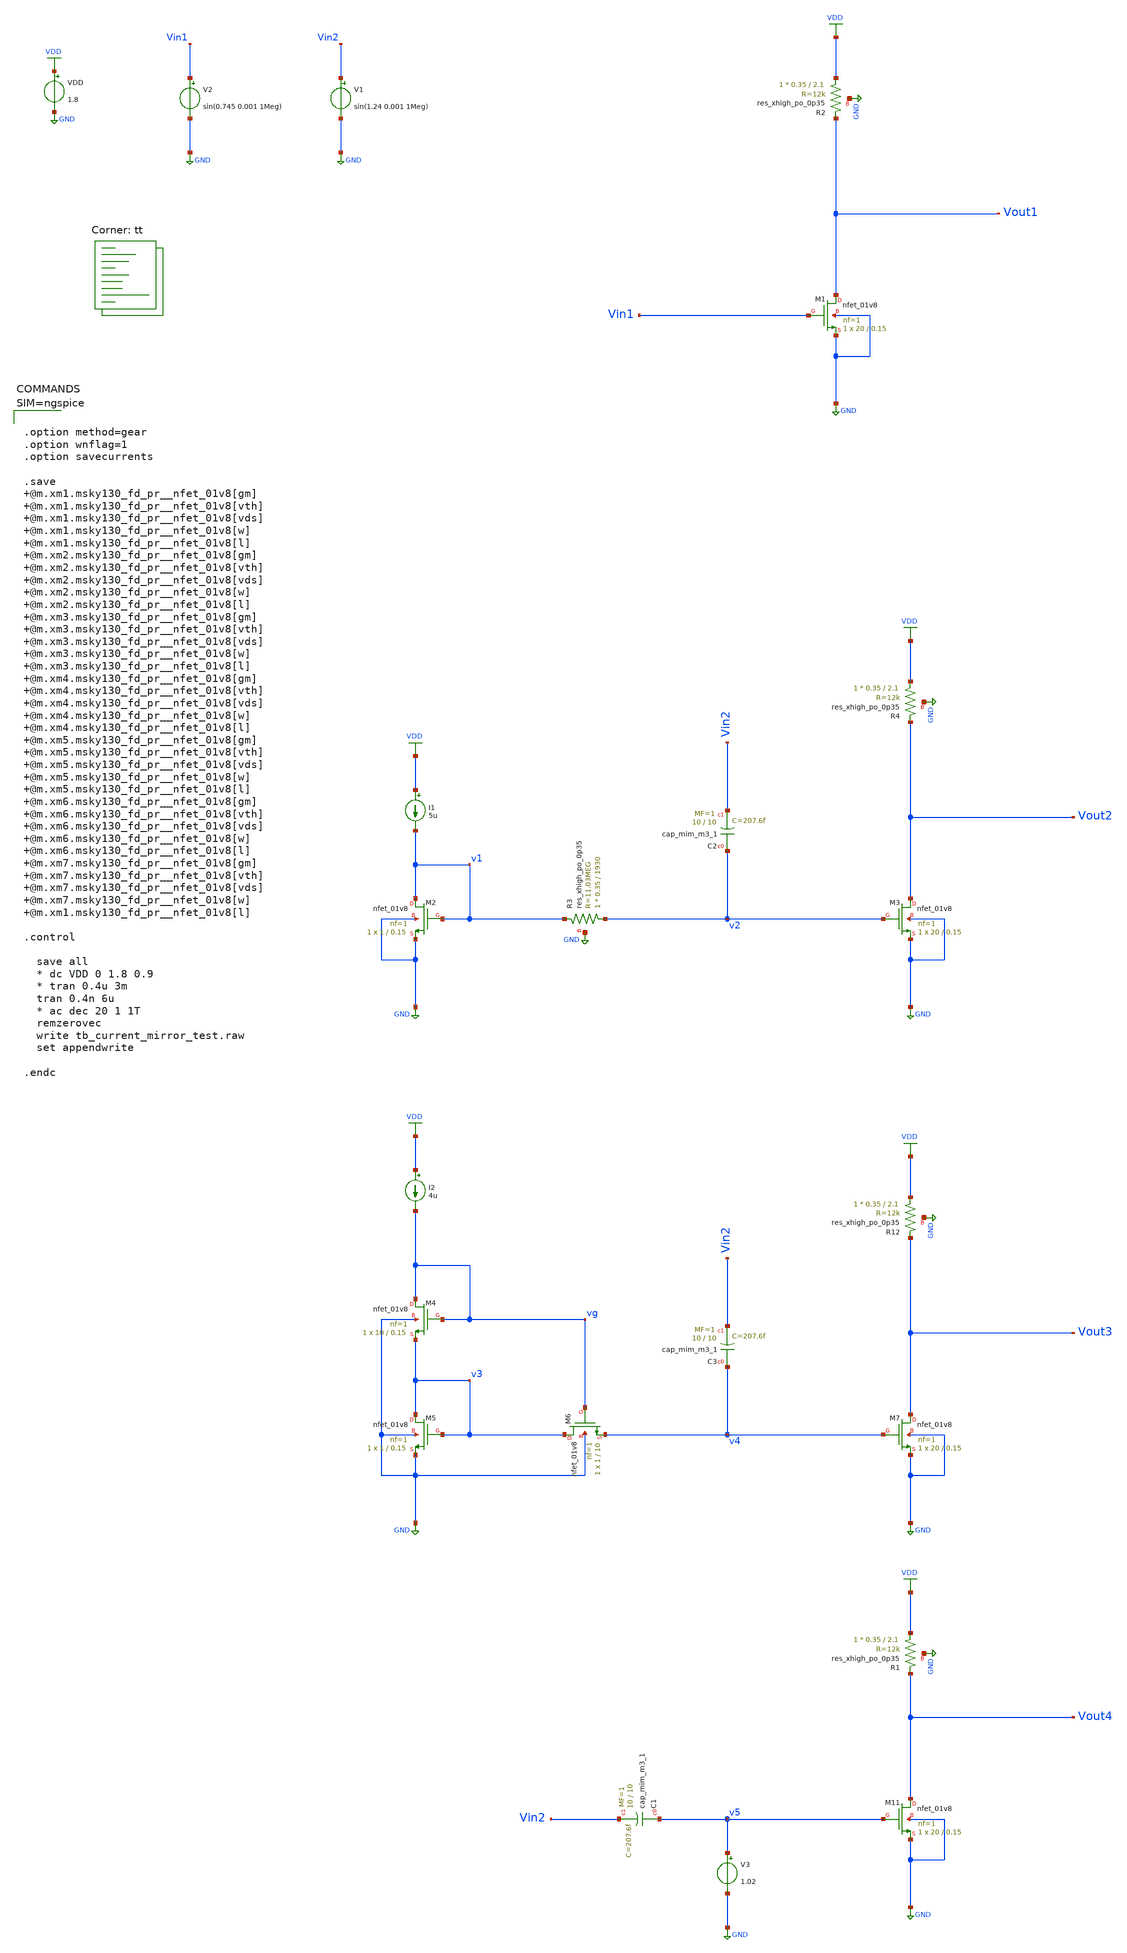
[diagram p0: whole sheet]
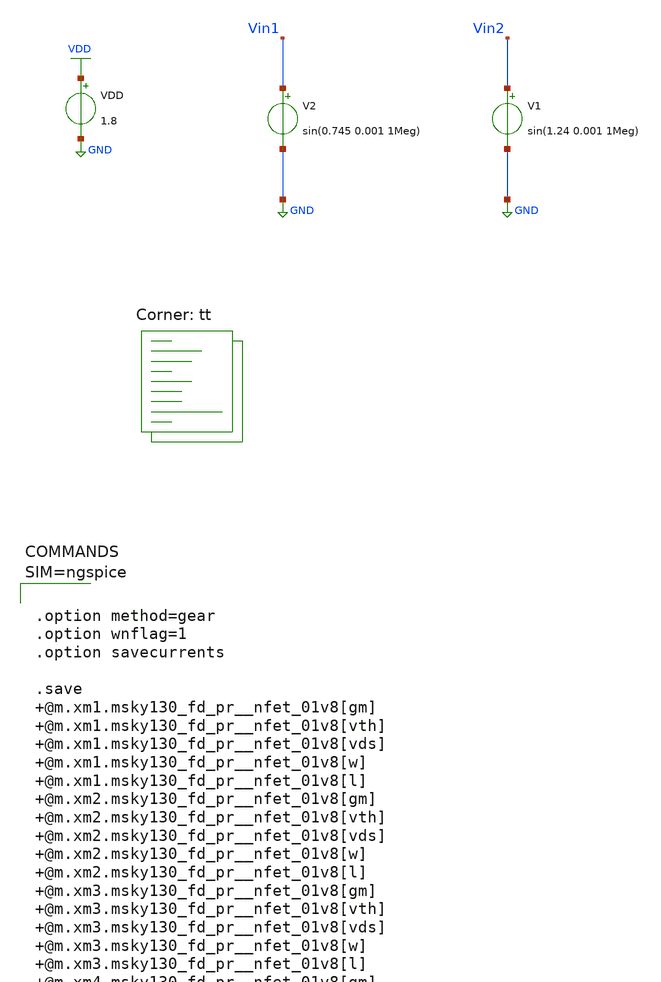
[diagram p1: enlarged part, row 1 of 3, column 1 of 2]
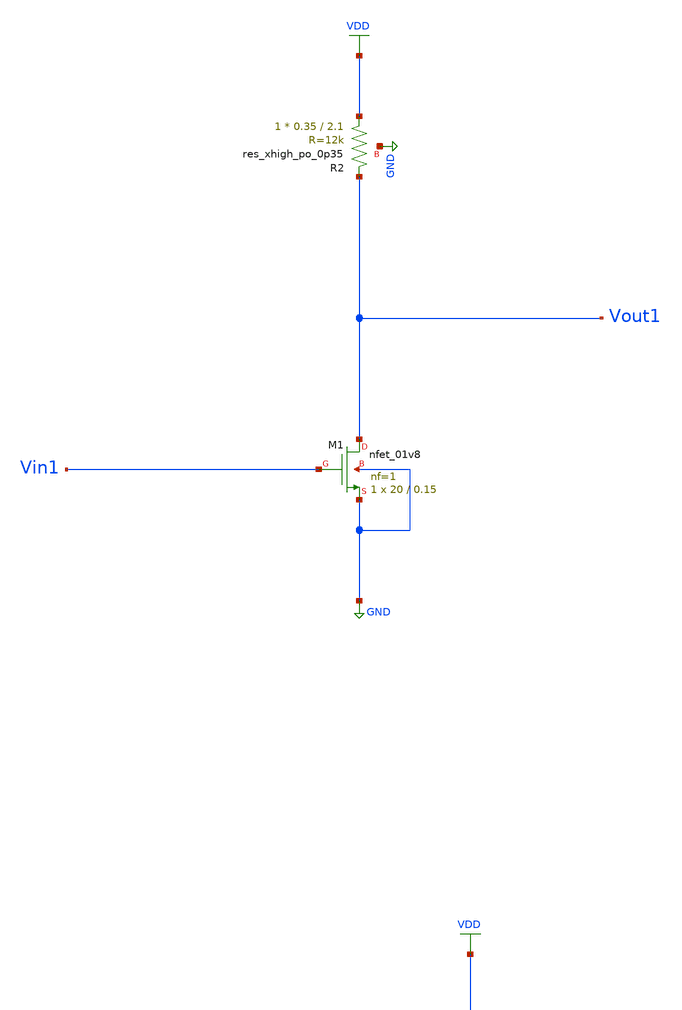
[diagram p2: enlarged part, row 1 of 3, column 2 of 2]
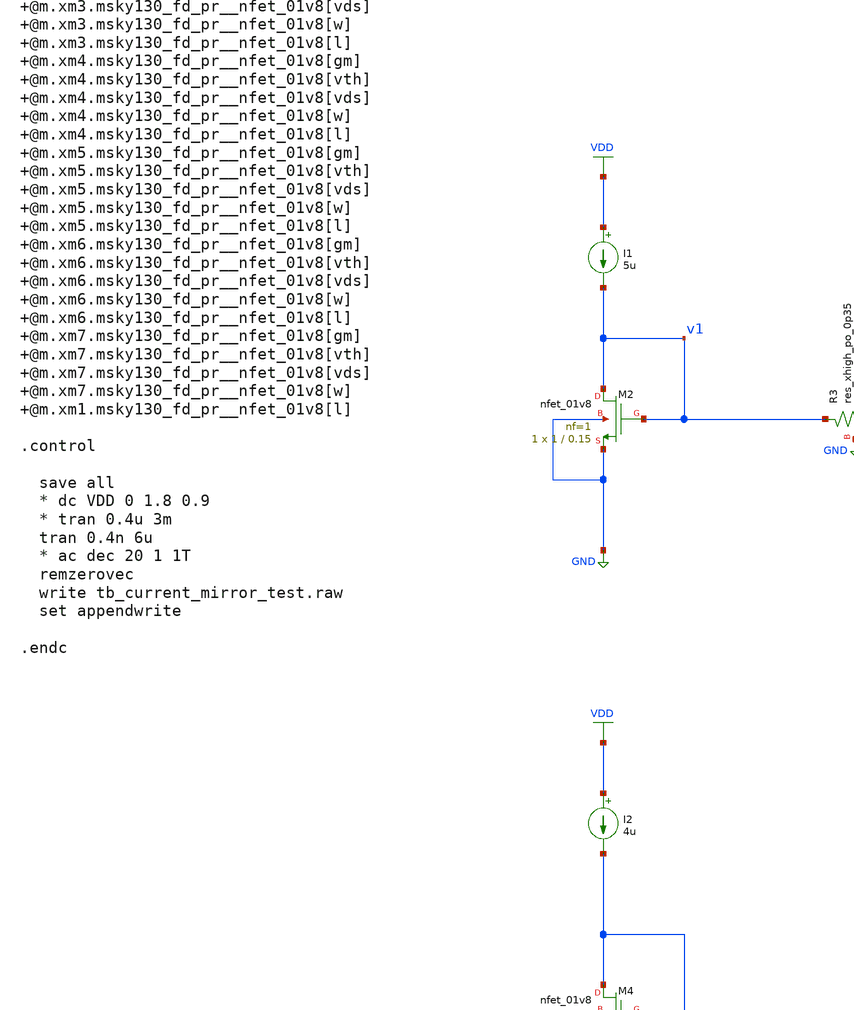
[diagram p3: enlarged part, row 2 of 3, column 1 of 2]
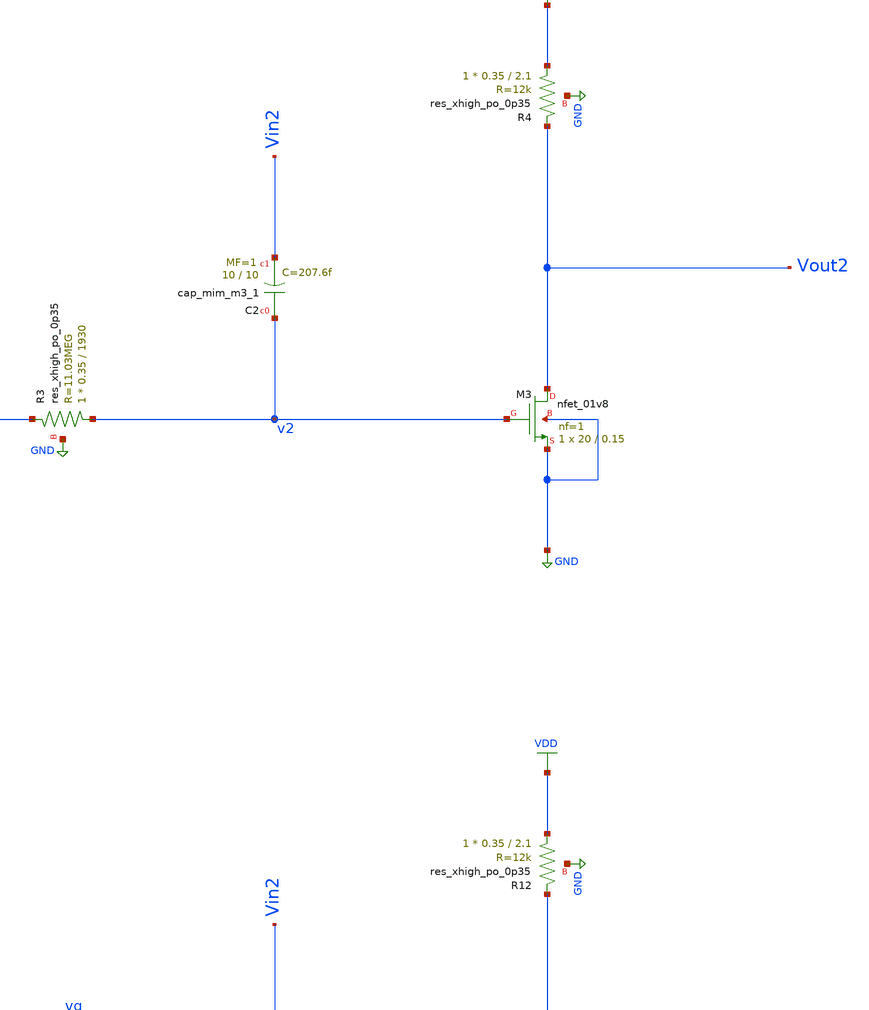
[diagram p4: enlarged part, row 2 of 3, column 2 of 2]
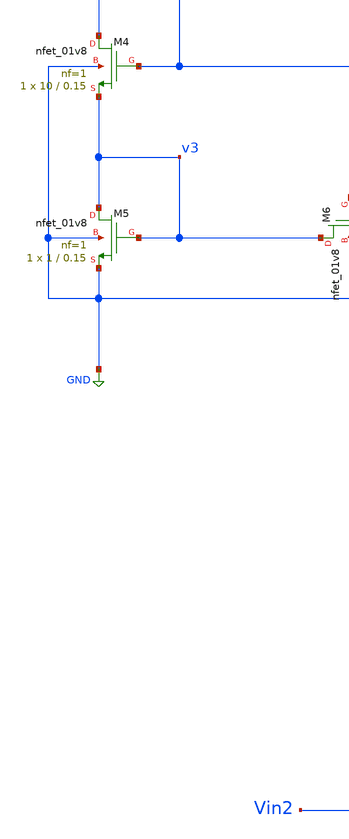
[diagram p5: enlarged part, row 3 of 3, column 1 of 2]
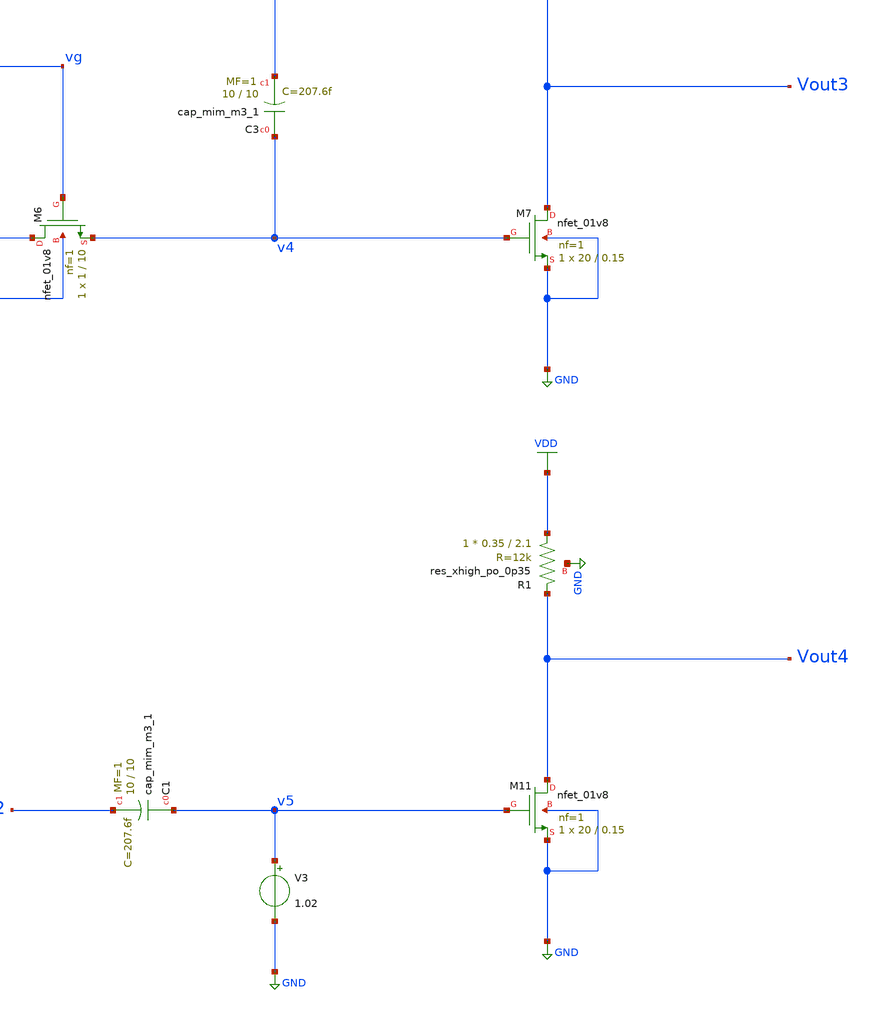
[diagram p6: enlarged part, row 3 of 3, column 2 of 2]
** sch_path: projects/opamp/xschem_ngspice/tb_current_mirror_test.sch
**.subckt tb_current_mirror_test
XM1 Vout1 Vin1 GND GND sky130_fd_pr__nfet_01v8 L=0.15 W=20 nf=1 ad='int((nf+1)/2) * W/nf * 0.29' as='int((nf+2)/2) * W/nf * 0.29'
+ pd='2*int((nf+1)/2) * (W/nf + 0.29)' ps='2*int((nf+2)/2) * (W/nf + 0.29)' nrd='0.29 / W' nrs='0.29 / W'
+ sa=0 sb=0 sd=0 mult=1 m=1
XR2 VDD Vout1 GND sky130_fd_pr__res_xhigh_po_0p35 L=2.1 mult=1 m=1
V2 Vin1 GND sin(0.745 0.001 1Meg)
VDD VDD GND 1.8
I2 VDD vg 4u
XR12 VDD Vout3 GND sky130_fd_pr__res_xhigh_po_0p35 L=2.1 mult=1 m=1
XC3 v4 Vin2 sky130_fd_pr__cap_mim_m3_1 W=10 L=10 MF=1 m=1
I1 VDD v1 5u
XM2 v1 v1 GND GND sky130_fd_pr__nfet_01v8 L=0.15 W=1 nf=1 ad='int((nf+1)/2) * W/nf * 0.29' as='int((nf+2)/2) * W/nf * 0.29'
+ pd='2*int((nf+1)/2) * (W/nf + 0.29)' ps='2*int((nf+2)/2) * (W/nf + 0.29)' nrd='0.29 / W' nrs='0.29 / W'
+ sa=0 sb=0 sd=0 mult=1 m=1
XR3 v2 v1 GND sky130_fd_pr__res_xhigh_po_0p35 L=1930 mult=1 m=1
XM3 Vout2 v2 GND GND sky130_fd_pr__nfet_01v8 L=0.15 W=20 nf=1 ad='int((nf+1)/2) * W/nf * 0.29' as='int((nf+2)/2) * W/nf * 0.29'
+ pd='2*int((nf+1)/2) * (W/nf + 0.29)' ps='2*int((nf+2)/2) * (W/nf + 0.29)' nrd='0.29 / W' nrs='0.29 / W'
+ sa=0 sb=0 sd=0 mult=1 m=1
XR4 VDD Vout2 GND sky130_fd_pr__res_xhigh_po_0p35 L=2.1 mult=1 m=1
XC2 v2 Vin2 sky130_fd_pr__cap_mim_m3_1 W=10 L=10 MF=1 m=1
XM4 vg vg v3 GND sky130_fd_pr__nfet_01v8 L=0.15 W=10 nf=1 ad='int((nf+1)/2) * W/nf * 0.29' as='int((nf+2)/2) * W/nf * 0.29'
+ pd='2*int((nf+1)/2) * (W/nf + 0.29)' ps='2*int((nf+2)/2) * (W/nf + 0.29)' nrd='0.29 / W' nrs='0.29 / W'
+ sa=0 sb=0 sd=0 mult=1 m=1
XM5 v3 v3 GND GND sky130_fd_pr__nfet_01v8 L=0.15 W=1 nf=1 ad='int((nf+1)/2) * W/nf * 0.29' as='int((nf+2)/2) * W/nf * 0.29'
+ pd='2*int((nf+1)/2) * (W/nf + 0.29)' ps='2*int((nf+2)/2) * (W/nf + 0.29)' nrd='0.29 / W' nrs='0.29 / W'
+ sa=0 sb=0 sd=0 mult=1 m=1
XM6 v3 vg v4 GND sky130_fd_pr__nfet_01v8 L=10 W=1 nf=1 ad='int((nf+1)/2) * W/nf * 0.29' as='int((nf+2)/2) * W/nf * 0.29'
+ pd='2*int((nf+1)/2) * (W/nf + 0.29)' ps='2*int((nf+2)/2) * (W/nf + 0.29)' nrd='0.29 / W' nrs='0.29 / W'
+ sa=0 sb=0 sd=0 mult=1 m=1
XM7 Vout3 v4 GND GND sky130_fd_pr__nfet_01v8 L=0.15 W=20 nf=1 ad='int((nf+1)/2) * W/nf * 0.29' as='int((nf+2)/2) * W/nf * 0.29'
+ pd='2*int((nf+1)/2) * (W/nf + 0.29)' ps='2*int((nf+2)/2) * (W/nf + 0.29)' nrd='0.29 / W' nrs='0.29 / W'
+ sa=0 sb=0 sd=0 mult=1 m=1
V1 Vin2 GND sin(1.24 0.001 1Meg)
XR1 VDD Vout4 GND sky130_fd_pr__res_xhigh_po_0p35 L=2.1 mult=1 m=1
XC1 v5 Vin2 sky130_fd_pr__cap_mim_m3_1 W=10 L=10 MF=1 m=1
XM11 Vout4 v5 GND GND sky130_fd_pr__nfet_01v8 L=0.15 W=20 nf=1 ad='int((nf+1)/2) * W/nf * 0.29' as='int((nf+2)/2) * W/nf * 0.29'
+ pd='2*int((nf+1)/2) * (W/nf + 0.29)' ps='2*int((nf+2)/2) * (W/nf + 0.29)' nrd='0.29 / W' nrs='0.29 / W'
+ sa=0 sb=0 sd=0 mult=1 m=1
V3 v5 GND 1.02
**** begin user architecture code



.option method=gear
.option wnflag=1
.option savecurrents

.save @m.xm1.msky130_fd_pr__nfet_01v8[gm] @m.xm1.msky130_fd_pr__nfet_01v8[vth] @m.xm1.msky130_fd_pr__nfet_01v8[vds] @m.xm1.msky130_fd_pr__nfet_01v8[w] @m.xm1.msky130_fd_pr__nfet_01v8[l] @m.xm2.msky130_fd_pr__nfet_01v8[gm] @m.xm2.msky130_fd_pr__nfet_01v8[vth] @m.xm2.msky130_fd_pr__nfet_01v8[vds] @m.xm2.msky130_fd_pr__nfet_01v8[w] @m.xm2.msky130_fd_pr__nfet_01v8[l] @m.xm3.msky130_fd_pr__nfet_01v8[gm] @m.xm3.msky130_fd_pr__nfet_01v8[vth] @m.xm3.msky130_fd_pr__nfet_01v8[vds] @m.xm3.msky130_fd_pr__nfet_01v8[w] @m.xm3.msky130_fd_pr__nfet_01v8[l] @m.xm4.msky130_fd_pr__nfet_01v8[gm] @m.xm4.msky130_fd_pr__nfet_01v8[vth] @m.xm4.msky130_fd_pr__nfet_01v8[vds] @m.xm4.msky130_fd_pr__nfet_01v8[w] @m.xm4.msky130_fd_pr__nfet_01v8[l] @m.xm5.msky130_fd_pr__nfet_01v8[gm] @m.xm5.msky130_fd_pr__nfet_01v8[vth] @m.xm5.msky130_fd_pr__nfet_01v8[vds] @m.xm5.msky130_fd_pr__nfet_01v8[w] @m.xm5.msky130_fd_pr__nfet_01v8[l] @m.xm6.msky130_fd_pr__nfet_01v8[gm] @m.xm6.msky130_fd_pr__nfet_01v8[vth] @m.xm6.msky130_fd_pr__nfet_01v8[vds] @m.xm6.msky130_fd_pr__nfet_01v8[w] @m.xm6.msky130_fd_pr__nfet_01v8[l] @m.xm7.msky130_fd_pr__nfet_01v8[gm] @m.xm7.msky130_fd_pr__nfet_01v8[vth] @m.xm7.msky130_fd_pr__nfet_01v8[vds] @m.xm7.msky130_fd_pr__nfet_01v8[w] @m.xm1.msky130_fd_pr__nfet_01v8[l]

.control

  save all
  * dc VDD 0 1.8 0.9
  * tran 0.4u 3m
  tran 0.4n 6u
  * ac dec 20 1 1T
  remzerovec
  write tb_current_mirror_test.raw
  set appendwrite

.endc




.lib $::SKYWATER_MODELS/sky130.lib.spice tt
**** end user architecture code
**.ends
.GLOBAL GND
.GLOBAL VDD
.end
